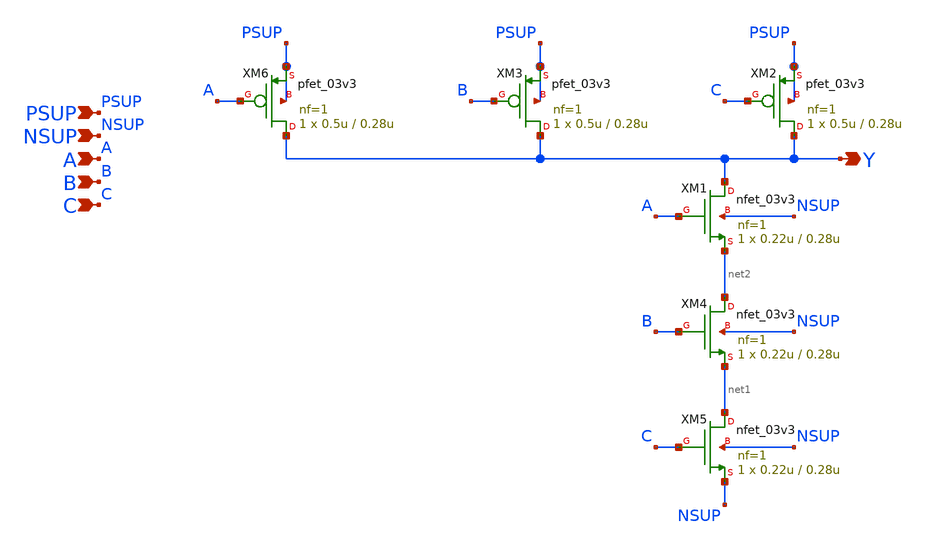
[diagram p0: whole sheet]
** sch_path: xschem/blocks/nand_3/nand_3.sch
**.subckt nand_3 PSUP NSUP A B Y C
*.ipin PSUP
*.ipin NSUP
*.ipin A
*.ipin B
*.opin Y
*.ipin C
XM5 net1 C NSUP NSUP nfet_03v3 L=0.28u W=0.22u nf=1 ad='int((nf+1)/2) * W/nf * 0.18u' as='int((nf+2)/2) * W/nf * 0.18u'
+ pd='2*int((nf+1)/2) * (W/nf + 0.18u)' ps='2*int((nf+2)/2) * (W/nf + 0.18u)' nrd='0.18u / W' nrs='0.18u / W'
+ sa=0 sb=0 sd=0 m=1
XM1 Y A net2 NSUP nfet_03v3 L=0.28u W=0.22u nf=1 ad='int((nf+1)/2) * W/nf * 0.18u' as='int((nf+2)/2) * W/nf * 0.18u'
+ pd='2*int((nf+1)/2) * (W/nf + 0.18u)' ps='2*int((nf+2)/2) * (W/nf + 0.18u)' nrd='0.18u / W' nrs='0.18u / W'
+ sa=0 sb=0 sd=0 m=1
XM2 Y C PSUP PSUP pfet_03v3 L=0.28u W=0.5u nf=1 ad='int((nf+1)/2) * W/nf * 0.18u' as='int((nf+2)/2) * W/nf * 0.18u'
+ pd='2*int((nf+1)/2) * (W/nf + 0.18u)' ps='2*int((nf+2)/2) * (W/nf + 0.18u)' nrd='0.18u / W' nrs='0.18u / W'
+ sa=0 sb=0 sd=0 m=1
XM3 Y B PSUP PSUP pfet_03v3 L=0.28u W=0.5u nf=1 ad='int((nf+1)/2) * W/nf * 0.18u' as='int((nf+2)/2) * W/nf * 0.18u'
+ pd='2*int((nf+1)/2) * (W/nf + 0.18u)' ps='2*int((nf+2)/2) * (W/nf + 0.18u)' nrd='0.18u / W' nrs='0.18u / W'
+ sa=0 sb=0 sd=0 m=1
XM4 net2 B net1 NSUP nfet_03v3 L=0.28u W=0.22u nf=1 ad='int((nf+1)/2) * W/nf * 0.18u' as='int((nf+2)/2) * W/nf * 0.18u'
+ pd='2*int((nf+1)/2) * (W/nf + 0.18u)' ps='2*int((nf+2)/2) * (W/nf + 0.18u)' nrd='0.18u / W' nrs='0.18u / W'
+ sa=0 sb=0 sd=0 m=1
XM6 Y A PSUP PSUP pfet_03v3 L=0.28u W=0.5u nf=1 ad='int((nf+1)/2) * W/nf * 0.18u' as='int((nf+2)/2) * W/nf * 0.18u'
+ pd='2*int((nf+1)/2) * (W/nf + 0.18u)' ps='2*int((nf+2)/2) * (W/nf + 0.18u)' nrd='0.18u / W' nrs='0.18u / W'
+ sa=0 sb=0 sd=0 m=1
**.ends
.end
